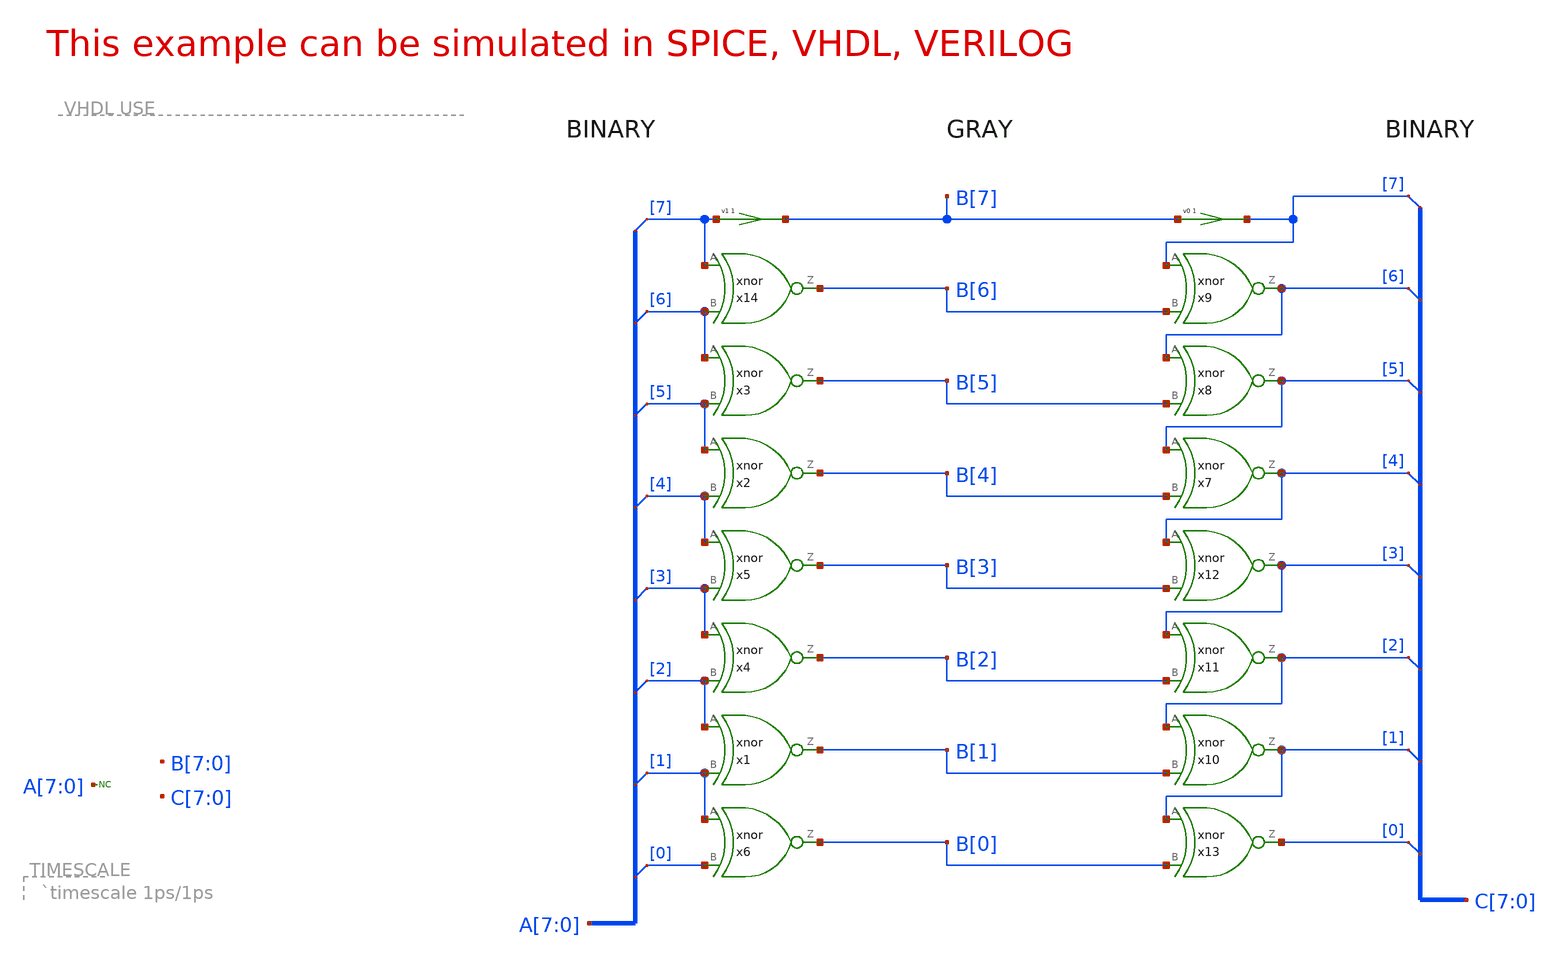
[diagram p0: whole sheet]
** sch_path: xschem-src/xschem_library/examples/greycnt.sch
* Copyright (C) 1998-2026 Stefan Frederik Schippers
* This program is free software; you can redistribute it and/or modify
* it under the terms of the GNU General Public License as published by
* the Free Software Foundation; either version 2 of the License, or
* (at your option) any later version.
* This program is distributed in the hope that it will be useful,
* but WITHOUT ANY WARRANTY; without even the implied warranty of
* MERCHANTABILITY or FITNESS FOR A PARTICULAR PURPOSE.  See the
* GNU General Public License for more details.
* You should have received a copy of the GNU General Public License
* along with this program; if not, write to the Free Software
**.subckt greycnt
x2 B[4] A[5] A[4] xnor
x3 B[5] A[6] A[5] xnor
x14 B[6] A[7] A[6] xnor
v1 B[7] A[7] 0
x1 B[1] A[2] A[1] xnor
x4 B[2] A[3] A[2] xnor
x5 B[3] A[4] A[3] xnor
x6 B[0] A[1] A[0] xnor
x7 C[4] C[5] B[4] xnor
x8 C[5] C[6] B[5] xnor
x9 C[6] C[7] B[6] xnor
v0 C[7] B[7] 0
x10 C[1] C[2] B[1] xnor
x11 C[2] C[3] B[2] xnor
x12 C[3] C[4] B[3] xnor
x13 C[0] C[1] B[0] xnor
* noconn A[7:0]
* tap: C[7:0] --> C[0]
* tap: C[7:0] --> C[1]
* tap: C[7:0] --> C[2]
* tap: C[7:0] --> C[3]
* tap: C[7:0] --> C[4]
* tap: C[7:0] --> C[5]
* tap: C[7:0] --> C[6]
* tap: C[7:0] --> C[7]
* tap: A[7:0] --> A[0]
* tap: A[7:0] --> A[1]
* tap: A[7:0] --> A[2]
* tap: A[7:0] --> A[3]
* tap: A[7:0] --> A[4]
* tap: A[7:0] --> A[5]
* tap: A[7:0] --> A[6]
* tap: A[7:0] --> A[7]
**** begin user architecture code



* ngspice commands
.options save all
.control
  tran 1n 2000n
  remzerovec
  write greycnt.raw
.endc

* to generate following file copy .../share/doc/xschem/examples/stimuli.greycnt
* to the simulation directory and run simulation -> Utile Stimuli Editor (GUI),
* and press 'Translate'
.include stimuli_greycnt.cir

.model nmos nmos level=49 version=3.3.0 vth0=0.8
.model pmos pmos level=49 version=3.3.0 vth0=-0.8






**** end user architecture code
**.ends

* expanding   symbol:  xnor.sym # of pins=3
** sym_path: xschem-src/xschem_library/examples/xnor.sym
** sch_path: xschem-src/xschem_library/examples/xnor.sch
.subckt xnor Z A B  risedel=400 falldel=300
*.ipin B
*.opin Z
*.ipin A
M1 net2 A GND GND nmos w=10u l=1u m=1
M2 net3 net1 GND GND nmos w=10u l=1u m=1
M3 Z A net3 GND nmos w=10u l=1u m=1
M4 Z B net3 GND nmos w=10u l=1u m=1
M5 net1 B net2 GND nmos w=10u l=1u m=1
M6 net1 A VDD VDD pmos w=10u l=1u m=1
M7 net1 B VDD VDD pmos w=10u l=1u m=1
M8 net4 A VDD VDD pmos w=10u l=1u m=1
M9 Z B net4 VDD pmos w=10u l=1u m=1
M10 Z net1 VDD VDD pmos w=10u l=1u m=1
.ends

.GLOBAL GND
.GLOBAL VDD
.end
